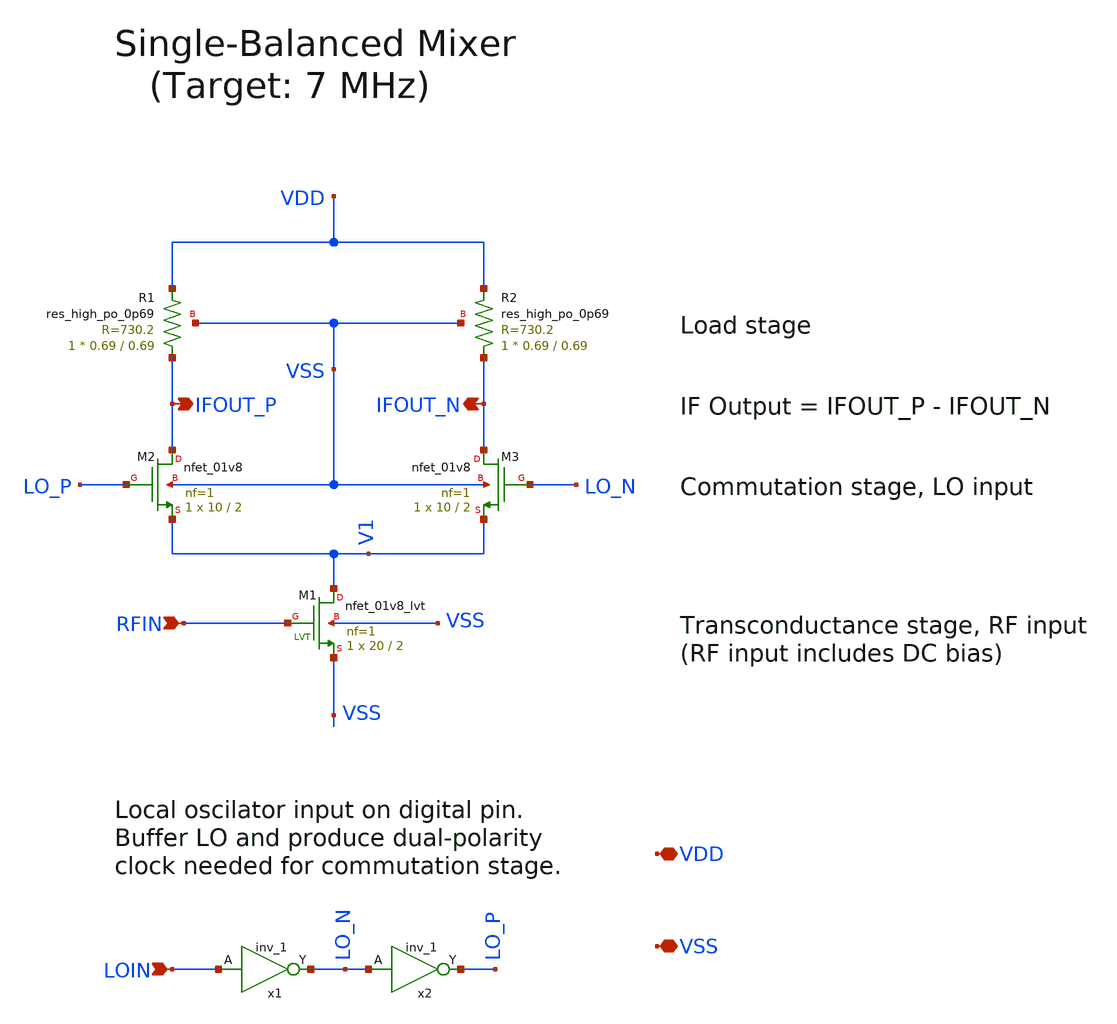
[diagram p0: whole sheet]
** sch_path: xschem/sb_mixer.sch
**.subckt sb_mixer VDD VSS LOIN RFIN IFOUT_P IFOUT_N
*.iopin VDD
*.iopin VSS
*.ipin LOIN
*.ipin RFIN
*.opin IFOUT_P
*.opin IFOUT_N
x1 LOIN VSS VSS VDD VDD LO_N sky130_fd_sc_hd__inv_1
x2 LO_N VSS VSS VDD VDD LO_P sky130_fd_sc_hd__inv_1
XM1 V1 RFIN VSS VSS sky130_fd_pr__nfet_01v8_lvt L=2 W=20 nf=1 ad='int((nf+1)/2) * W/nf * 0.29' as='int((nf+2)/2) * W/nf * 0.29'
+ pd='2*int((nf+1)/2) * (W/nf + 0.29)' ps='2*int((nf+2)/2) * (W/nf + 0.29)' nrd='0.29 / W' nrs='0.29 / W'
+ sa=0 sb=0 sd=0 mult=1 m=1
XM2 IFOUT_P LO_P V1 VSS sky130_fd_pr__nfet_01v8 L=2 W=10 nf=1 ad='int((nf+1)/2) * W/nf * 0.29' as='int((nf+2)/2) * W/nf * 0.29'
+ pd='2*int((nf+1)/2) * (W/nf + 0.29)' ps='2*int((nf+2)/2) * (W/nf + 0.29)' nrd='0.29 / W' nrs='0.29 / W'
+ sa=0 sb=0 sd=0 mult=1 m=1
XM3 IFOUT_N LO_N V1 VSS sky130_fd_pr__nfet_01v8 L=2 W=10 nf=1 ad='int((nf+1)/2) * W/nf * 0.29' as='int((nf+2)/2) * W/nf * 0.29'
+ pd='2*int((nf+1)/2) * (W/nf + 0.29)' ps='2*int((nf+2)/2) * (W/nf + 0.29)' nrd='0.29 / W' nrs='0.29 / W'
+ sa=0 sb=0 sd=0 mult=1 m=1
XR1 IFOUT_P VDD VSS sky130_fd_pr__res_high_po_0p69 L=0.69 mult=1 m=1
XR2 IFOUT_N VDD VSS sky130_fd_pr__res_high_po_0p69 L=0.69 mult=1 m=1
**.ends
.end
